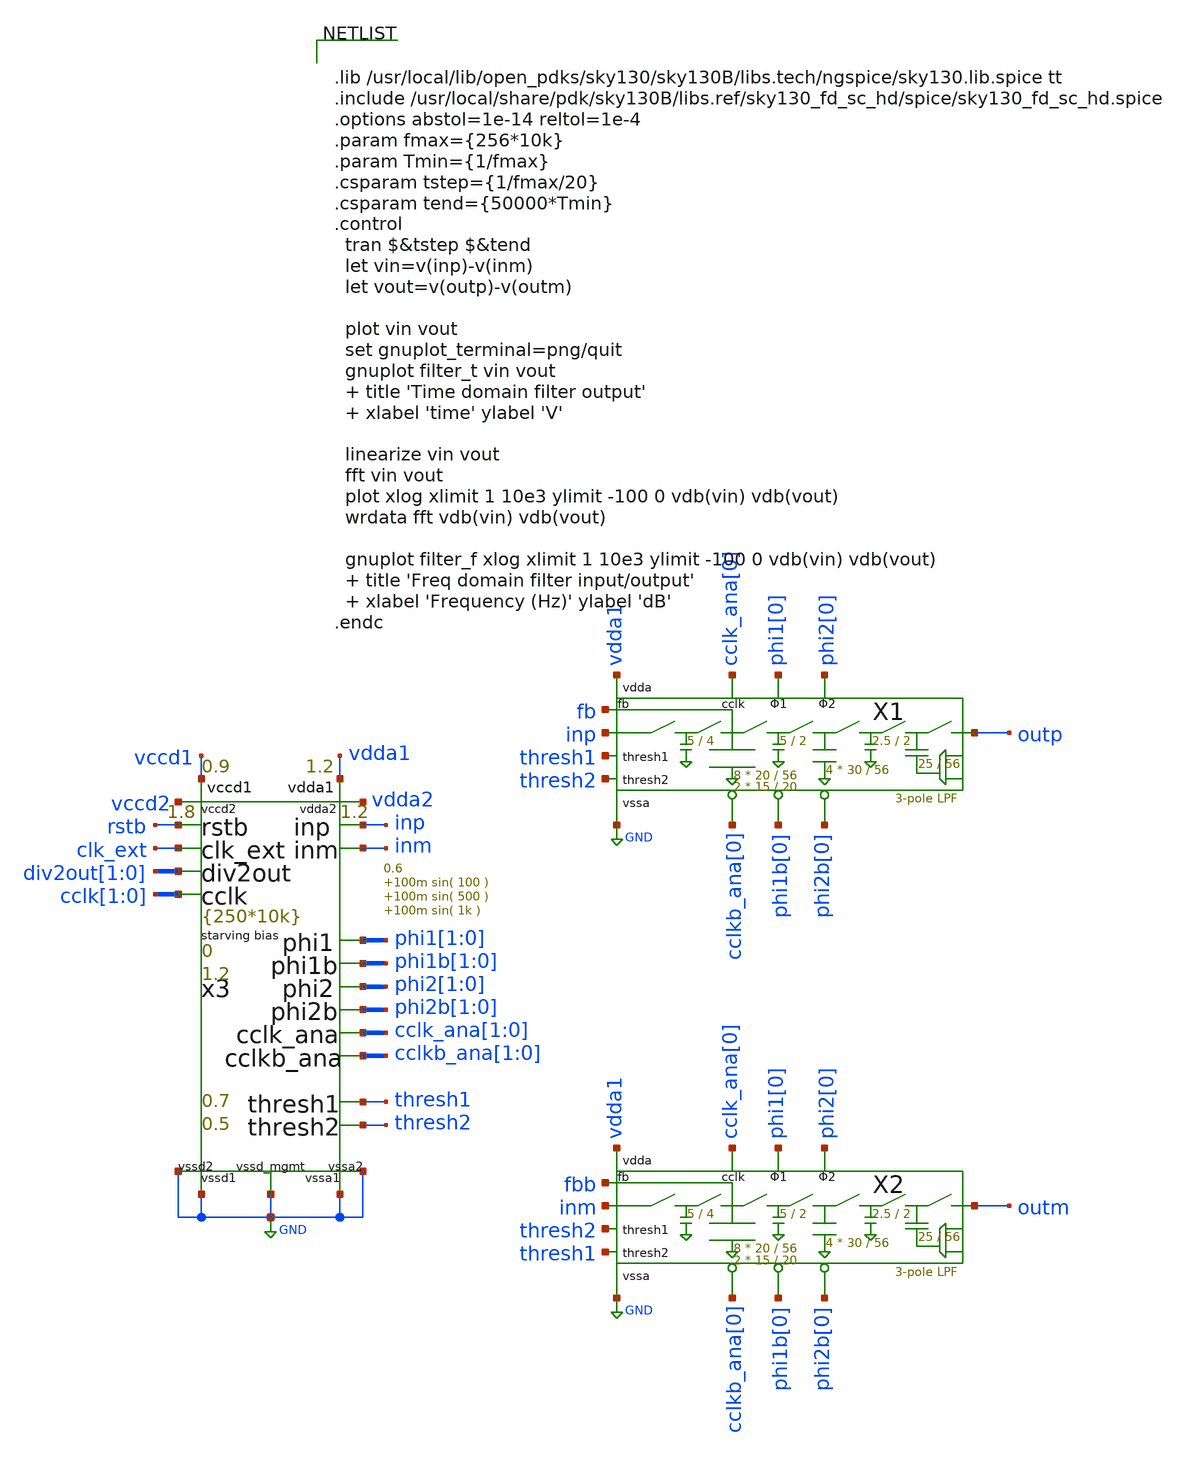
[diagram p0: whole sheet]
** sch_path: xschem/test_bench/filter_tb.sch
**.subckt filter_tb
X1 inp outp phi2[0] phi1[0] phi1b[0] phi2b[0] cclk_ana[0] cclkb_ana[0] thresh1 thresh2 vdda1 GND fb
+ filter WC1=20 LC1=56 WC1B=15 LC1B=20 WC2=30 LC2=56 WC3=25 LC3=56 WCS1=5 LCS1=4 WCS2=5 LCS2=2 WCS3=2.5
+ LCS3=2
X2 inm outm phi2[0] phi1[0] phi1b[0] phi2b[0] cclk_ana[0] cclkb_ana[0] thresh2 thresh1 vdda1 GND fbb
+ filter WC1=20 LC1=56 WC1B=15 LC1B=20 WC2=30 LC2=56 WC3=25 LC3=56 WCS1=5 LCS1=4 WCS2=5 LCS2=2 WCS3=2.5
+ LCS3=2
x3 thresh1 thresh2 inp inm clk_ext rstb phi1[1] phi1[0] phi1b[1] phi1b[0] phi2[1] phi2[0] phi2b[1] phi2b[0]
+ cclk_ana[1] cclk_ana[0] cclkb_ana[1] cclkb_ana[0] div2out[1] div2out[0] cclk[1] cclk[0] vdda1 vccd1 vccd2
+ vdda2 GND GND GND GND GND risc_signals p_vdda1=1.2 p_vdda2=1.2 p_vccd1=0.9 p_vccd2=1.8 p_vccd_mgmt=1.8
+ p_fclk={250*10k} p_duty_cycle=0.5 p_rstb_delay={1.5/p_fclk} p_rstb_tr=5n p_thresh1=0.7 p_thresh2=0.5
+ p_vpb=0 p_vnb=1.2 p_vcm=0.6 p_amp1=100m p_f1=100 p_amp2=100m p_f2=500 p_amp3=100m p_f3=1k
**** begin user architecture code


.lib /usr/local/lib/open_pdks/sky130/sky130B/libs.tech/ngspice/sky130.lib.spice tt
.include /usr/local/share/pdk/sky130B/libs.ref/sky130_fd_sc_hd/spice/sky130_fd_sc_hd.spice
.options abstol=1e-14 reltol=1e-4
.param fmax={256*10k}
.param Tmin={1/fmax}
.csparam tstep={1/fmax/20}
.csparam tend={50000*Tmin}
.control
  tran $&tstep $&tend
  let vin=v(inp)-v(inm)
  let vout=v(outp)-v(outm)

  plot vin vout
  set gnuplot_terminal=png/quit
  gnuplot filter_t vin vout
  + title 'Time domain filter output'
  + xlabel 'time' ylabel 'V'

  linearize vin vout
  fft vin vout
  plot xlog xlimit 1 10e3 ylimit -100 0 vdb(vin) vdb(vout)
  wrdata fft vdb(vin) vdb(vout)

  gnuplot filter_f xlog xlimit 1 10e3 ylimit -100 0 vdb(vin) vdb(vout)
  + title 'Freq domain filter input/output'
  + xlabel 'Frequency (Hz)' ylabel 'dB'
.endc


**** end user architecture code
**.ends
.GLOBAL GND
.end
